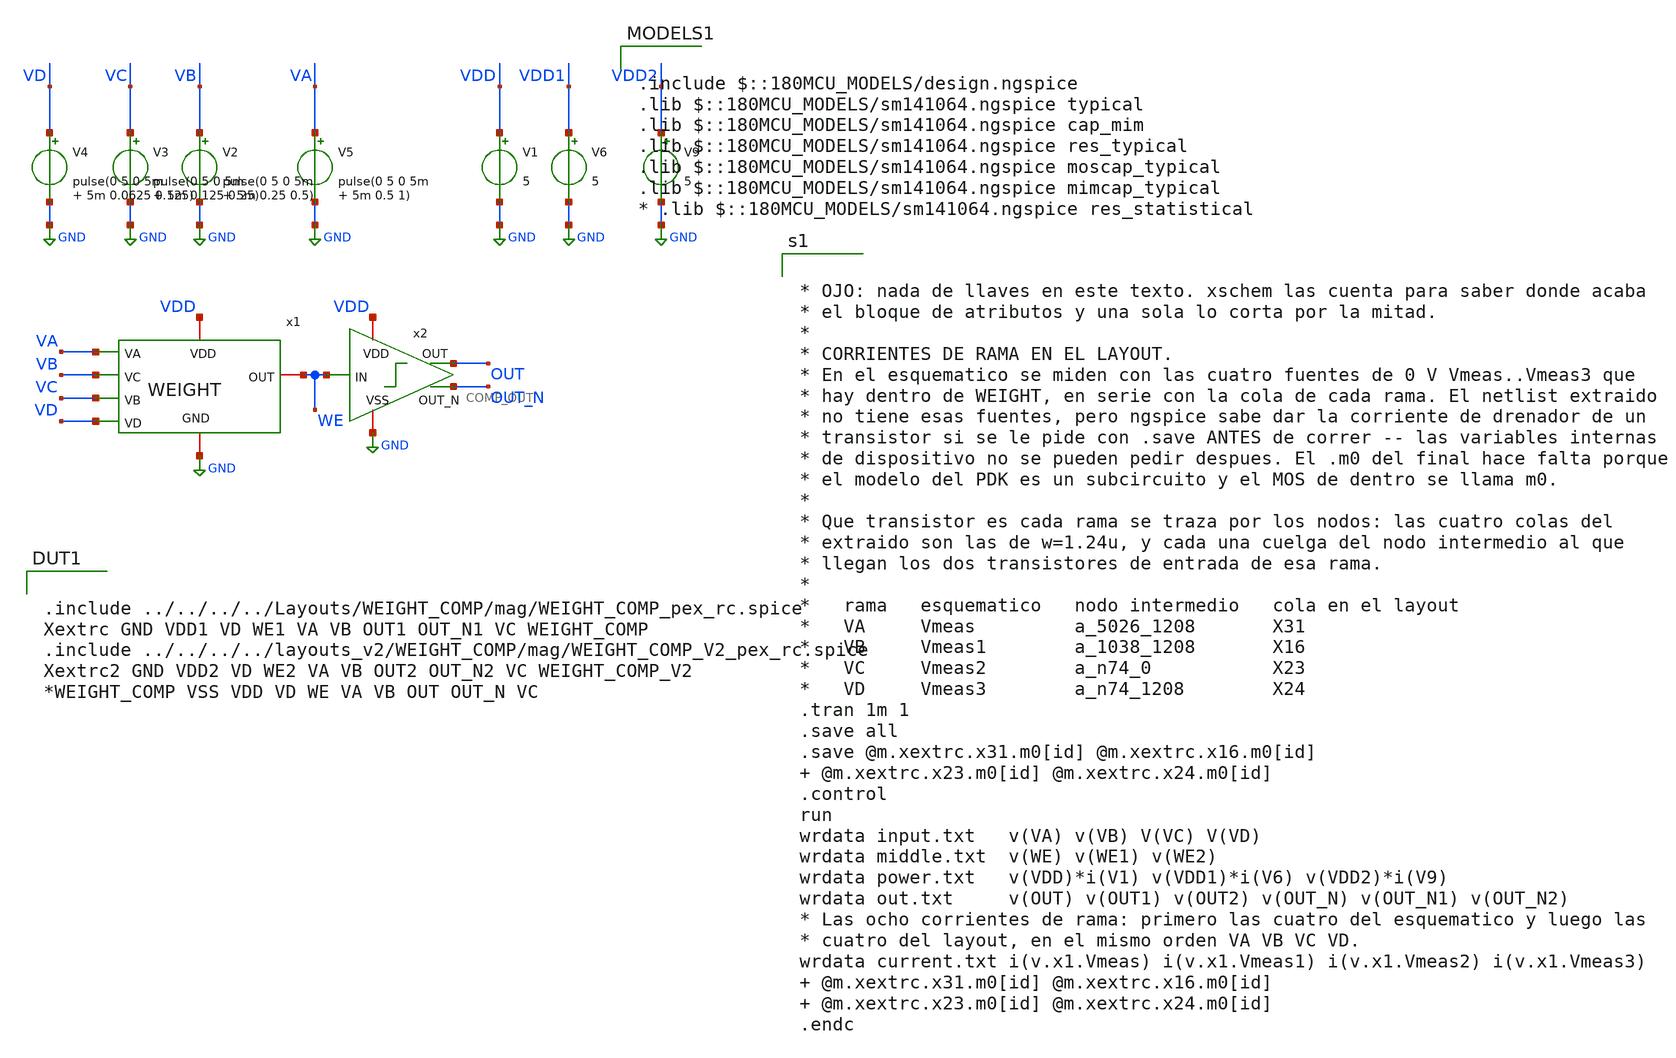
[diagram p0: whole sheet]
** sch_path: FINAL/XSCHEM/TEST/test_weight.sch
**.subckt test_weight
V1 VDD GND 5
V5 VA GND pulse(0 5 0 5m 5m 0.5 1)
x1 VDD GND WE VA VB VC VD WEIGHT
x2 VDD OUT WE OUT_N GND COMP_OUT
V6 VDD1 GND 5
V9 VDD2 GND 5
V2 VB GND pulse(0 5 0 5m 5m 0.25 0.5)
V3 VC GND pulse(0 5 0 5m 5m 0.125 0.25)
V4 VD GND pulse(0 5 0 5m 5m 0.0625 0.125)
**** begin user architecture code


* OJO: nada de llaves en este texto. xschem las cuenta para saber donde acaba
* el bloque de atributos y una sola lo corta por la mitad.
*
* CORRIENTES DE RAMA EN EL LAYOUT.
* En el esquematico se miden con las cuatro fuentes de 0 V Vmeas..Vmeas3 que
* hay dentro de WEIGHT, en serie con la cola de cada rama. El netlist extraido
* no tiene esas fuentes, pero ngspice sabe dar la corriente de drenador de un
* transistor si se le pide con .save ANTES de correr -- las variables internas
* de dispositivo no se pueden pedir despues. El .m0 del final hace falta porque
* el modelo del PDK es un subcircuito y el MOS de dentro se llama m0.
*
* Que transistor es cada rama se traza por los nodos: las cuatro colas del
* extraido son las de w=1.24u, y cada una cuelga del nodo intermedio al que
* llegan los dos transistores de entrada de esa rama.
*
*   rama   esquematico   nodo intermedio   cola en el layout
*   VA     Vmeas         a_5026_1208       X31
*   VB     Vmeas1        a_1038_1208       X16
*   VC     Vmeas2        a_n74_0           X23
*   VD     Vmeas3        a_n74_1208        X24
.tran 1m 1
.save all
.save @m.xextrc.x31.m0[id] @m.xextrc.x16.m0[id]  @m.xextrc.x23.m0[id] @m.xextrc.x24.m0[id]
.control
run
wrdata input.txt   v(VA) v(VB) V(VC) V(VD)
wrdata middle.txt  v(WE) v(WE1) v(WE2)
wrdata power.txt   v(VDD)*i(V1) v(VDD1)*i(V6) v(VDD2)*i(V9)
wrdata out.txt     v(OUT) v(OUT1) v(OUT2) v(OUT_N) v(OUT_N1) v(OUT_N2)
* Las ocho corrientes de rama: primero las cuatro del esquematico y luego las
* cuatro del layout, en el mismo orden VA VB VC VD.
wrdata current.txt i(v.x1.Vmeas) i(v.x1.Vmeas1) i(v.x1.Vmeas2) i(v.x1.Vmeas3)  @m.xextrc.x31.m0[id]
+ @m.xextrc.x16.m0[id]  @m.xextrc.x23.m0[id] @m.xextrc.x24.m0[id]
.endc



.include $::180MCU_MODELS/design.ngspice
.lib $::180MCU_MODELS/sm141064.ngspice typical
.lib $::180MCU_MODELS/sm141064.ngspice cap_mim
.lib $::180MCU_MODELS/sm141064.ngspice res_typical
.lib $::180MCU_MODELS/sm141064.ngspice moscap_typical
.lib $::180MCU_MODELS/sm141064.ngspice mimcap_typical
* .lib $::180MCU_MODELS/sm141064.ngspice res_statistical


.include ../../../../Layouts/WEIGHT_COMP/mag/WEIGHT_COMP_pex_rc.spice
Xextrc GND VDD1 VD WE1 VA VB OUT1 OUT_N1 VC WEIGHT_COMP
.include ../../../../layouts_v2/WEIGHT_COMP/mag/WEIGHT_COMP_V2_pex_rc.spice
Xextrc2 GND VDD2 VD WE2 VA VB OUT2 OUT_N2 VC WEIGHT_COMP_V2
*WEIGHT_COMP VSS VDD VD WE VA VB OUT OUT_N VC

**** end user architecture code
**.ends
.GLOBAL GND
.end
